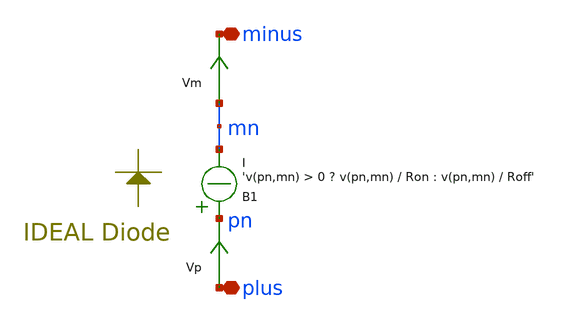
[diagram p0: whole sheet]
** sch_path: xschem_library_oa/ngspice/diode_ngspice/schematic/diode_ngspice.sch
* Copyright (C) 1998-2024 Stefan Frederik Schippers
* This program is free software; you can redistribute it and/or modify
* it under the terms of the GNU General Public License as published by
* the Free Software Foundation; either version 2 of the License, or
* (at your option) any later version.
* This program is distributed in the hope that it will be useful,
* but WITHOUT ANY WARRANTY; without even the implied warranty of
* MERCHANTABILITY or FITNESS FOR A PARTICULAR PURPOSE.  See the
* GNU General Public License for more details.
* You should have received a copy of the GNU General Public License
* along with this program; if not, write to the Free Software
**.subckt diode_ngspice plus minus
*.iopin plus
*.iopin minus
Vm mn minus 0
.save i(vm)
Vp plus pn 0
.save i(vp)
B1 pn mn I = 'v(pn,mn) > 0 ? v(pn,mn) / Ron : v(pn,mn) / Roff'
**.ends
.end
